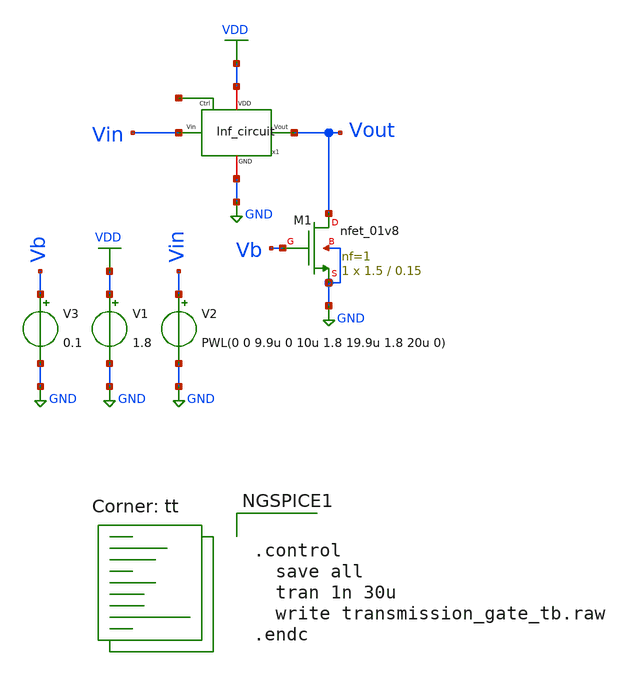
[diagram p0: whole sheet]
** sch_path: Final_Design/Inf_Circuit_tb.sch
**.subckt Inf_Circuit_tb
V1 VDD GND 1.8
V2 Vin GND PWL(0 0 9.9u 0 10u 1.8 19.9u 1.8 20u 0)
XM1 Vout Vb GND GND sky130_fd_pr__nfet_01v8 L=0.15 W=1.5 nf=1 ad='int((nf+1)/2) * W/nf * 0.29' as='int((nf+2)/2) * W/nf * 0.29'
+ pd='2*int((nf+1)/2) * (W/nf + 0.29)' ps='2*int((nf+2)/2) * (W/nf + 0.29)' nrd='0.29 / W' nrs='0.29 / W'
+ sa=0 sb=0 sd=0 mult=1 m=1
V3 Vb GND 0.1
x1 net1 Vin GND VDD Vout Inf_circuit
**** begin user architecture code
.lib $::SKYWATER_MODELS/sky130.lib.spice tt


.control
  save all
  tran 1n 30u
  write transmission_gate_tb.raw
.endc


**** end user architecture code
**.ends
.GLOBAL GND
.GLOBAL VDD
.end
